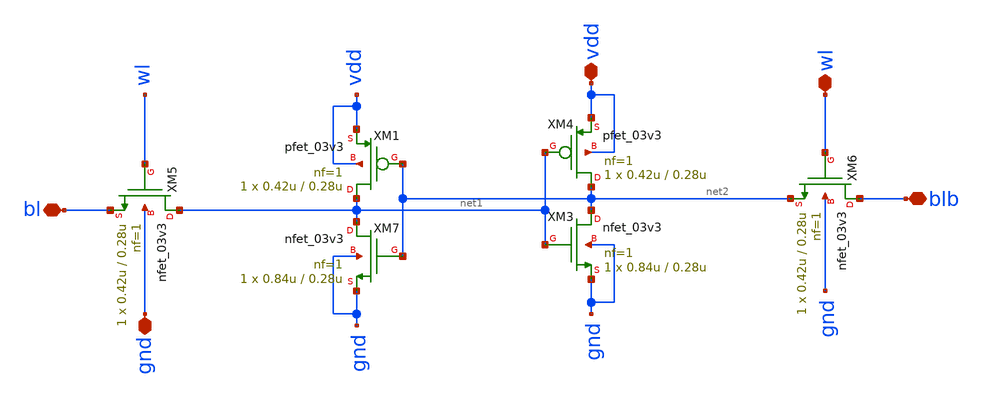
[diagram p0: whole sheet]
** sch_path: src/pixel/sram.sch
**.subckt sram vdd wl bl blb gnd
*.iopin vdd
*.iopin wl
*.iopin bl
*.iopin blb
*.iopin gnd
XM3 net2 net1 gnd gnd nfet_03v3 L=0.28u W=0.84u nf=1 ad='int((nf+1)/2) * W/nf * 0.18u' as='int((nf+2)/2) * W/nf * 0.18u'
+ pd='2*int((nf+1)/2) * (W/nf + 0.18u)' ps='2*int((nf+2)/2) * (W/nf + 0.18u)' nrd='0.18u / W' nrs='0.18u / W'
+ sa=0 sb=0 sd=0 m=1
XM4 net2 net1 vdd vdd pfet_03v3 L=0.28u W=0.42u nf=1 ad='int((nf+1)/2) * W/nf * 0.18u' as='int((nf+2)/2) * W/nf * 0.18u'
+ pd='2*int((nf+1)/2) * (W/nf + 0.18u)' ps='2*int((nf+2)/2) * (W/nf + 0.18u)' nrd='0.18u / W' nrs='0.18u / W'
+ sa=0 sb=0 sd=0 m=1
XM5 net1 wl bl gnd nfet_03v3 L=0.28u W=0.42u nf=1 ad='int((nf+1)/2) * W/nf * 0.18u' as='int((nf+2)/2) * W/nf * 0.18u'
+ pd='2*int((nf+1)/2) * (W/nf + 0.18u)' ps='2*int((nf+2)/2) * (W/nf + 0.18u)' nrd='0.18u / W' nrs='0.18u / W'
+ sa=0 sb=0 sd=0 m=1
XM6 blb wl net2 gnd nfet_03v3 L=0.28u W=0.42u nf=1 ad='int((nf+1)/2) * W/nf * 0.18u' as='int((nf+2)/2) * W/nf * 0.18u'
+ pd='2*int((nf+1)/2) * (W/nf + 0.18u)' ps='2*int((nf+2)/2) * (W/nf + 0.18u)' nrd='0.18u / W' nrs='0.18u / W'
+ sa=0 sb=0 sd=0 m=1
XM7 net1 net2 gnd gnd nfet_03v3 L=0.28u W=0.84u nf=1 ad='int((nf+1)/2) * W/nf * 0.18u' as='int((nf+2)/2) * W/nf * 0.18u'
+ pd='2*int((nf+1)/2) * (W/nf + 0.18u)' ps='2*int((nf+2)/2) * (W/nf + 0.18u)' nrd='0.18u / W' nrs='0.18u / W'
+ sa=0 sb=0 sd=0 m=1
XM1 net1 net2 vdd vdd pfet_03v3 L=0.28u W=0.42u nf=1 ad='int((nf+1)/2) * W/nf * 0.18u' as='int((nf+2)/2) * W/nf * 0.18u'
+ pd='2*int((nf+1)/2) * (W/nf + 0.18u)' ps='2*int((nf+2)/2) * (W/nf + 0.18u)' nrd='0.18u / W' nrs='0.18u / W'
+ sa=0 sb=0 sd=0 m=1
**.ends
.end
